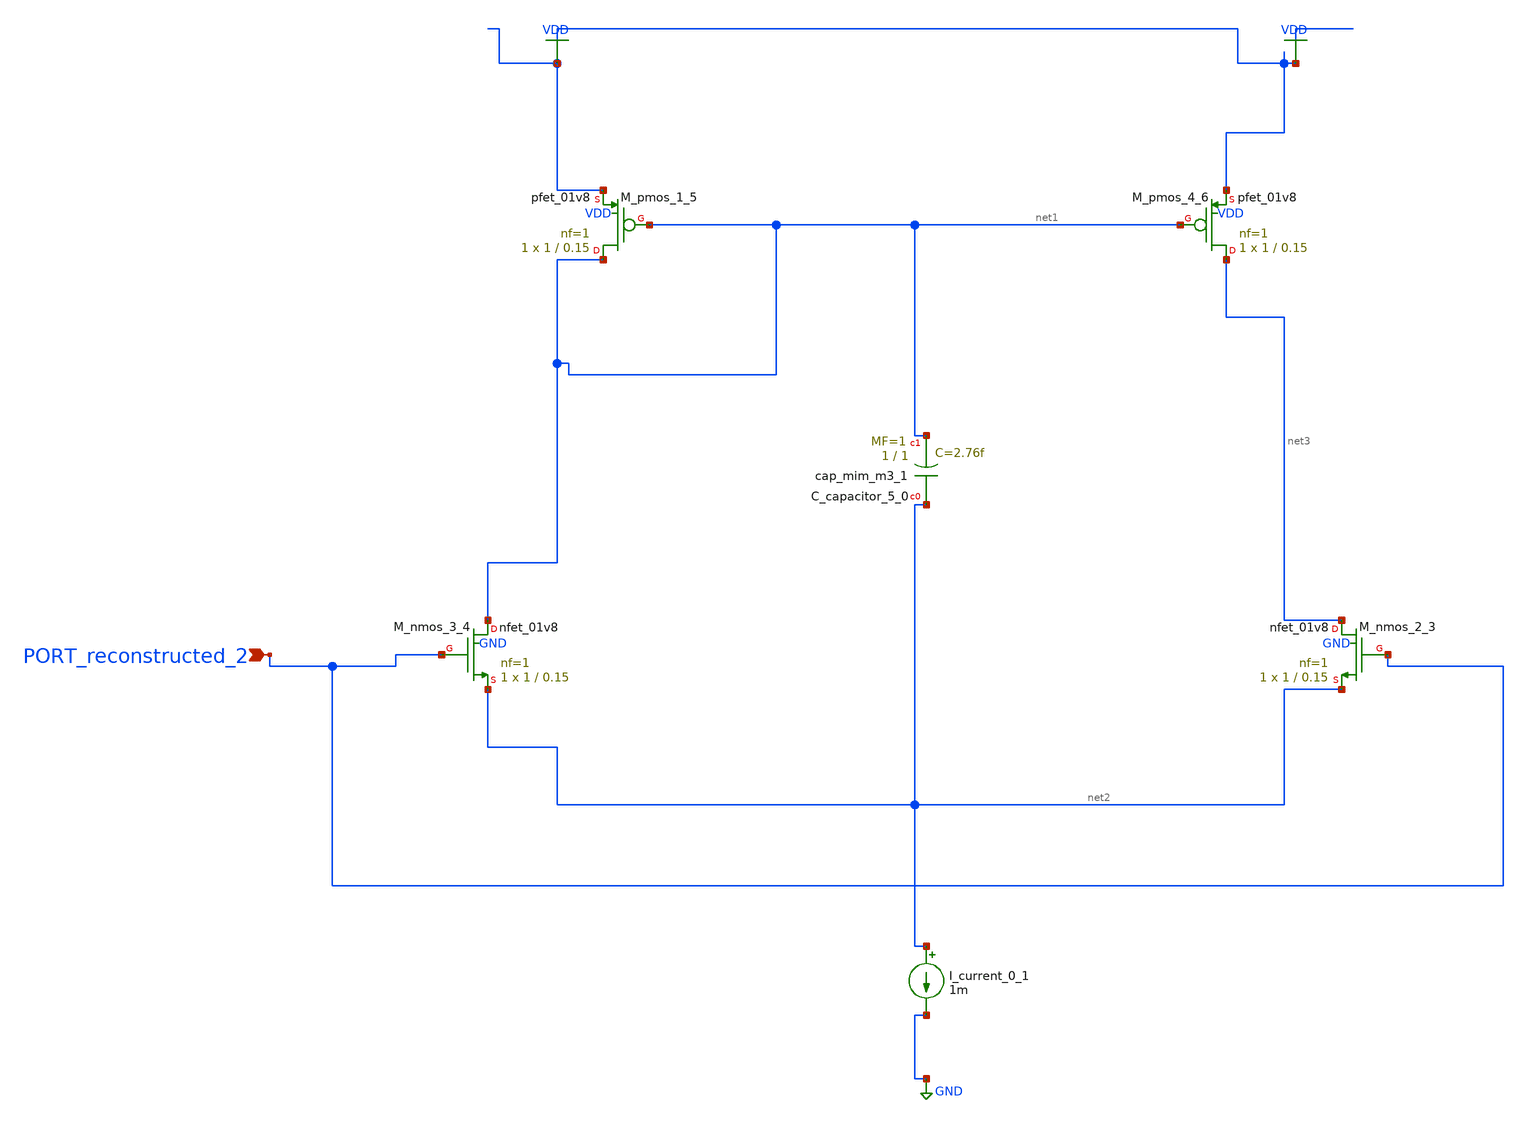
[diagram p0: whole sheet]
** sch_path: schematics/AMSNet/352.sch
**.subckt 352 PORT_reconstructed_2
*.ipin PORT_reconstructed_2
XC_capacitor_5_0 net2 net1 sky130_fd_pr__cap_mim_m3_1 W=1 L=1 MF=1 m=1
I_current_0_1 net2 GND 1m
XM_nmos_2_3 net3 PORT_reconstructed_2 net2 GND sky130_fd_pr__nfet_01v8 L=0.15 W=1 nf=1 ad='int((1 + 1)/2) * 1 / 1 * 0.29'
+ as='int((1 + 2)/2) * 1 / 1 * 0.29' pd='2*int((1 + 1)/2) * (1 / 1 + 0.29)' ps='2*int((1 + 2)/2) * (1 / 1 + 0.29)'
+ nrd='0.29 / 1 ' nrs='0.29 / 1 ' sa=0 sb=0 sd=0 mult=1 m=1
XM_nmos_3_4 net1 PORT_reconstructed_2 net2 GND sky130_fd_pr__nfet_01v8 L=0.15 W=1 nf=1 ad='int((1 + 1)/2) * 1 / 1 * 0.29'
+ as='int((1 + 2)/2) * 1 / 1 * 0.29' pd='2*int((1 + 1)/2) * (1 / 1 + 0.29)' ps='2*int((1 + 2)/2) * (1 / 1 + 0.29)'
+ nrd='0.29 / 1 ' nrs='0.29 / 1 ' sa=0 sb=0 sd=0 mult=1 m=1
XM_pmos_1_5 net1 net1 VDD VDD sky130_fd_pr__pfet_01v8 L=0.15 W=1 nf=1 ad='int((1 + 1)/2) * 1 / 1 * 0.29'
+ as='int((1 + 2)/2) * 1 / 1 * 0.29' pd='2*int((1 + 1)/2) * (1 / 1 + 0.29)' ps='2*int((1 + 2)/2) * (1 / 1 + 0.29)'
+ nrd='0.29 / 1 ' nrs='0.29 / 1 ' sa=0 sb=0 sd=0 mult=1 m=1
XM_pmos_4_6 net3 net1 VDD VDD sky130_fd_pr__pfet_01v8 L=0.15 W=1 nf=1 ad='int((1 + 1)/2) * 1 / 1 * 0.29'
+ as='int((1 + 2)/2) * 1 / 1 * 0.29' pd='2*int((1 + 1)/2) * (1 / 1 + 0.29)' ps='2*int((1 + 2)/2) * (1 / 1 + 0.29)'
+ nrd='0.29 / 1 ' nrs='0.29 / 1 ' sa=0 sb=0 sd=0 mult=1 m=1
**.ends
.GLOBAL GND
.GLOBAL VDD
.end
